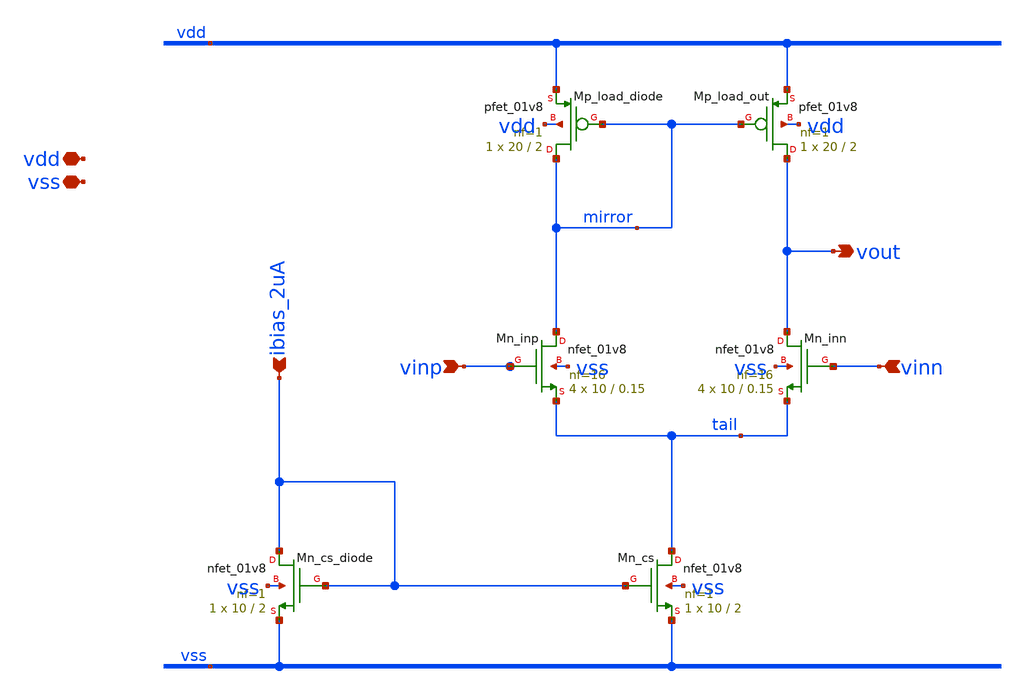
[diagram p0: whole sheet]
** sch_path: xsch/ip/otas/5T_OTA_1.sch
**.subckt 5T_OTA_1 vdd vss vinp vinn vout ibias_2uA
*.iopin vdd
*.iopin vss
*.ipin vinp
*.ipin vinn
*.opin vout
*.ipin ibias_2uA
XMn_inp mirror vinp tail vss sky130_fd_pr__nfet_01v8 L=0.15 W=10 nf=16 ad='int((16 + 1)/2) * 10 / 16 * 0.29'
+ as='int((16 + 2)/2) * 10 / 16 * 0.29' pd='2*int((16 + 1)/2) * (10 / 16 + 0.29)' ps='2*int((16 + 2)/2) * (10 / 16 + 0.29)'
+ nrd='0.29 / 10 ' nrs='0.29 / 10 ' sa=0 sb=0 sd=0 mult=4 m=4
XMn_inn vout vinn tail vss sky130_fd_pr__nfet_01v8 L=0.15 W=10 nf=16 ad='int((16 + 1)/2) * 10 / 16 * 0.29'
+ as='int((16 + 2)/2) * 10 / 16 * 0.29' pd='2*int((16 + 1)/2) * (10 / 16 + 0.29)' ps='2*int((16 + 2)/2) * (10 / 16 + 0.29)'
+ nrd='0.29 / 10 ' nrs='0.29 / 10 ' sa=0 sb=0 sd=0 mult=4 m=4
XMn_cs tail ibias_2uA vss vss sky130_fd_pr__nfet_01v8 L=2 W=10 nf=1 ad='int((1 + 1)/2) * 10 / 1 * 0.29'
+ as='int((1 + 2)/2) * 10 / 1 * 0.29' pd='2*int((1 + 1)/2) * (10 / 1 + 0.29)' ps='2*int((1 + 2)/2) * (10 / 1 + 0.29)'
+ nrd='0.29 / 10 ' nrs='0.29 / 10 ' sa=0 sb=0 sd=0 mult=1 m=1
XMp_load_out vout mirror vdd vdd sky130_fd_pr__pfet_01v8 L=2 W=20 nf=1 ad='int((nf+1)/2) * W/nf * 0.29'
+ as='int((nf+2)/2) * W/nf * 0.29' pd='2*int((nf+1)/2) * (W/nf + 0.29)' ps='2*int((nf+2)/2) * (W/nf + 0.29)'
+ nrd='0.29 / W' nrs='0.29 / W' sa=0 sb=0 sd=0 mult=1 m=1
XMp_load_diode mirror mirror vdd vdd sky130_fd_pr__pfet_01v8 L=2 W=20 nf=1 ad='int((nf+1)/2) * W/nf * 0.29'
+ as='int((nf+2)/2) * W/nf * 0.29' pd='2*int((nf+1)/2) * (W/nf + 0.29)' ps='2*int((nf+2)/2) * (W/nf + 0.29)'
+ nrd='0.29 / W' nrs='0.29 / W' sa=0 sb=0 sd=0 mult=1 m=1
XMn_cs_diode ibias_2uA ibias_2uA vss vss sky130_fd_pr__nfet_01v8 L=2 W=10 nf=1 ad='int((1 + 1)/2) * 10 / 1 * 0.29'
+ as='int((1 + 2)/2) * 10 / 1 * 0.29' pd='2*int((1 + 1)/2) * (10 / 1 + 0.29)' ps='2*int((1 + 2)/2) * (10 / 1 + 0.29)'
+ nrd='0.29 / 10 ' nrs='0.29 / 10 ' sa=0 sb=0 sd=0 mult=1 m=1
**.ends
.end
